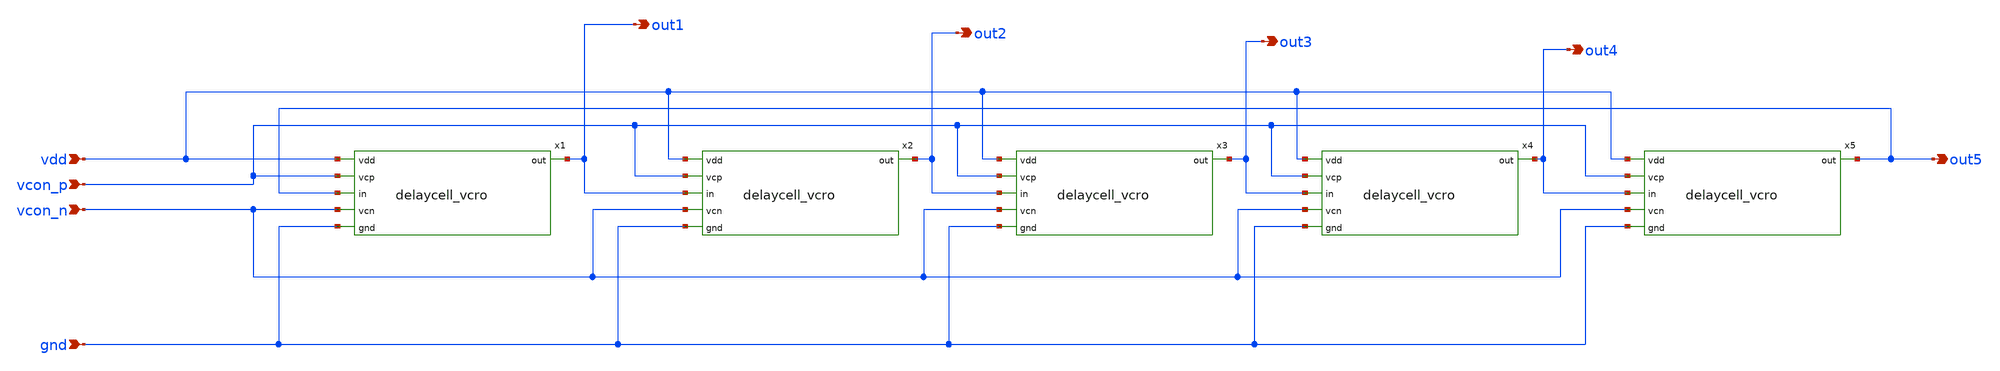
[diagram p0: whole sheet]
** sch_path: xschem/vcro_5elements_taps.sch
**.subckt vcro_5elements_taps vdd vcon_p vcon_n gnd out5 out4 out3 out2 out1
*.ipin vdd
*.ipin vcon_p
*.ipin vcon_n
*.ipin gnd
*.opin out5
*.opin out4
*.opin out3
*.opin out2
*.opin out1
x1 vdd vcon_p out1 out5 vcon_n gnd delaycell_vcro
x2 vdd vcon_p out2 out1 vcon_n gnd delaycell_vcro
x3 vdd vcon_p out3 out2 vcon_n gnd delaycell_vcro
x4 vdd vcon_p out4 out3 vcon_n gnd delaycell_vcro
x5 vdd vcon_p out5 out4 vcon_n gnd delaycell_vcro
**.ends
.end
